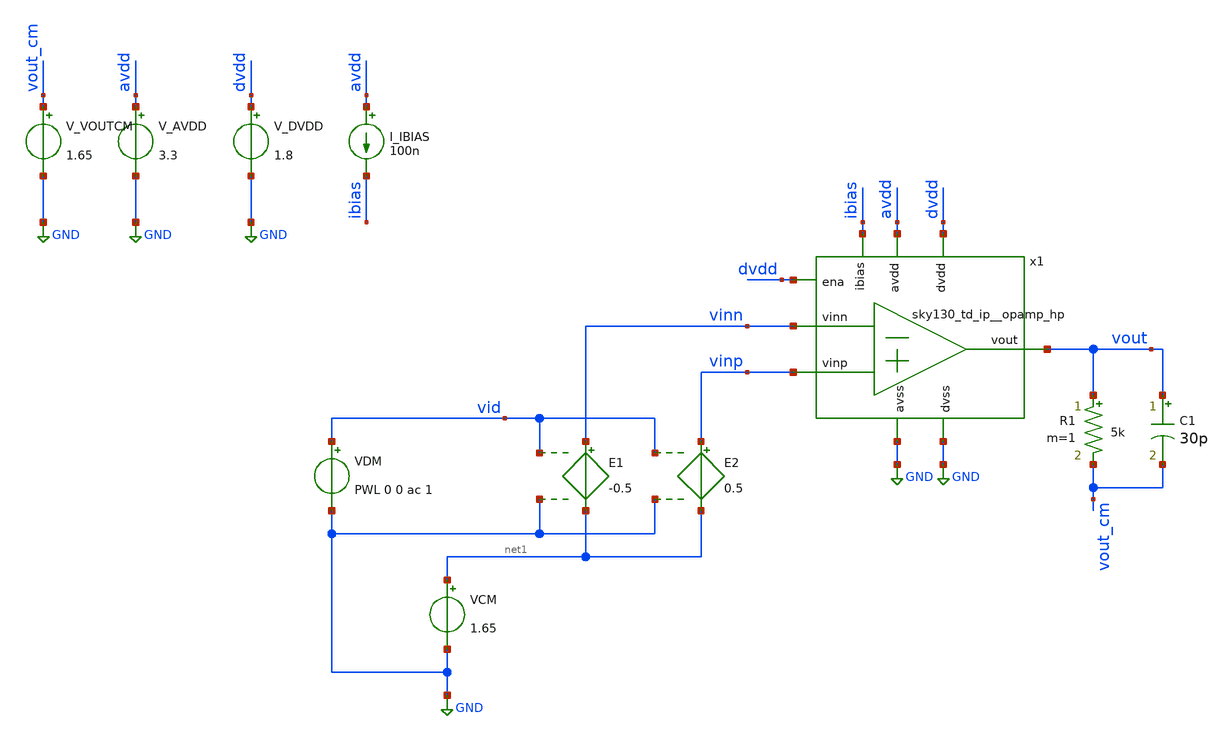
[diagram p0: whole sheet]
** sch_path: xschem/offset.sch
**.subckt offset
x1 avdd vout ibias vinn vinp GND dvdd GND dvdd sky130_td_ip__opamp_hp
V_AVDD avdd GND 3.3
.save i(v_avdd)
V_DVDD dvdd GND 1.8
.save i(v_dvdd)
I_IBIAS avdd ibias 100n
VCM net1 GND 1.65
R1 vout vout_cm 5k m=1
C1 vout vout_cm 30p m=1
V_VOUTCM vout_cm GND 1.65
.save i(v_voutcm)
E1 vinn net1 vid GND -0.5
VDM vid GND PWL 0 0 ac 1
E2 vinp net1 vid GND 0.5
**** begin user architecture code


.save all

.control
save all

alter @VDM[pwl] = [ 0 -10m 10 10m ]
tran 5m 10
run

let vid = v(vid)
let vout = v(vout)
meas tran input_offset_voltage FIND vid WHEN vout=1.65 RISE=LAST

echo
echo ===================================
echo Differential-mode DC sweep results
echo - Input Offset voltage: $&input_offset_voltage
echo ===================================

plot vout
*plot vid

alter @VDM[pwl] = [ 0 0 ]
alter @VDM[dc] = $&input_offset_voltage

ac DEC 10 1 1G
run

let gain_db = db(vout / vid)
plot gain_db


.endc




.option TEMP=-40
.lib /usr/local/share/pdk/sky130A/libs.tech/combined/sky130.lib.spice tt


**** end user architecture code
**.ends
.GLOBAL GND
.end
